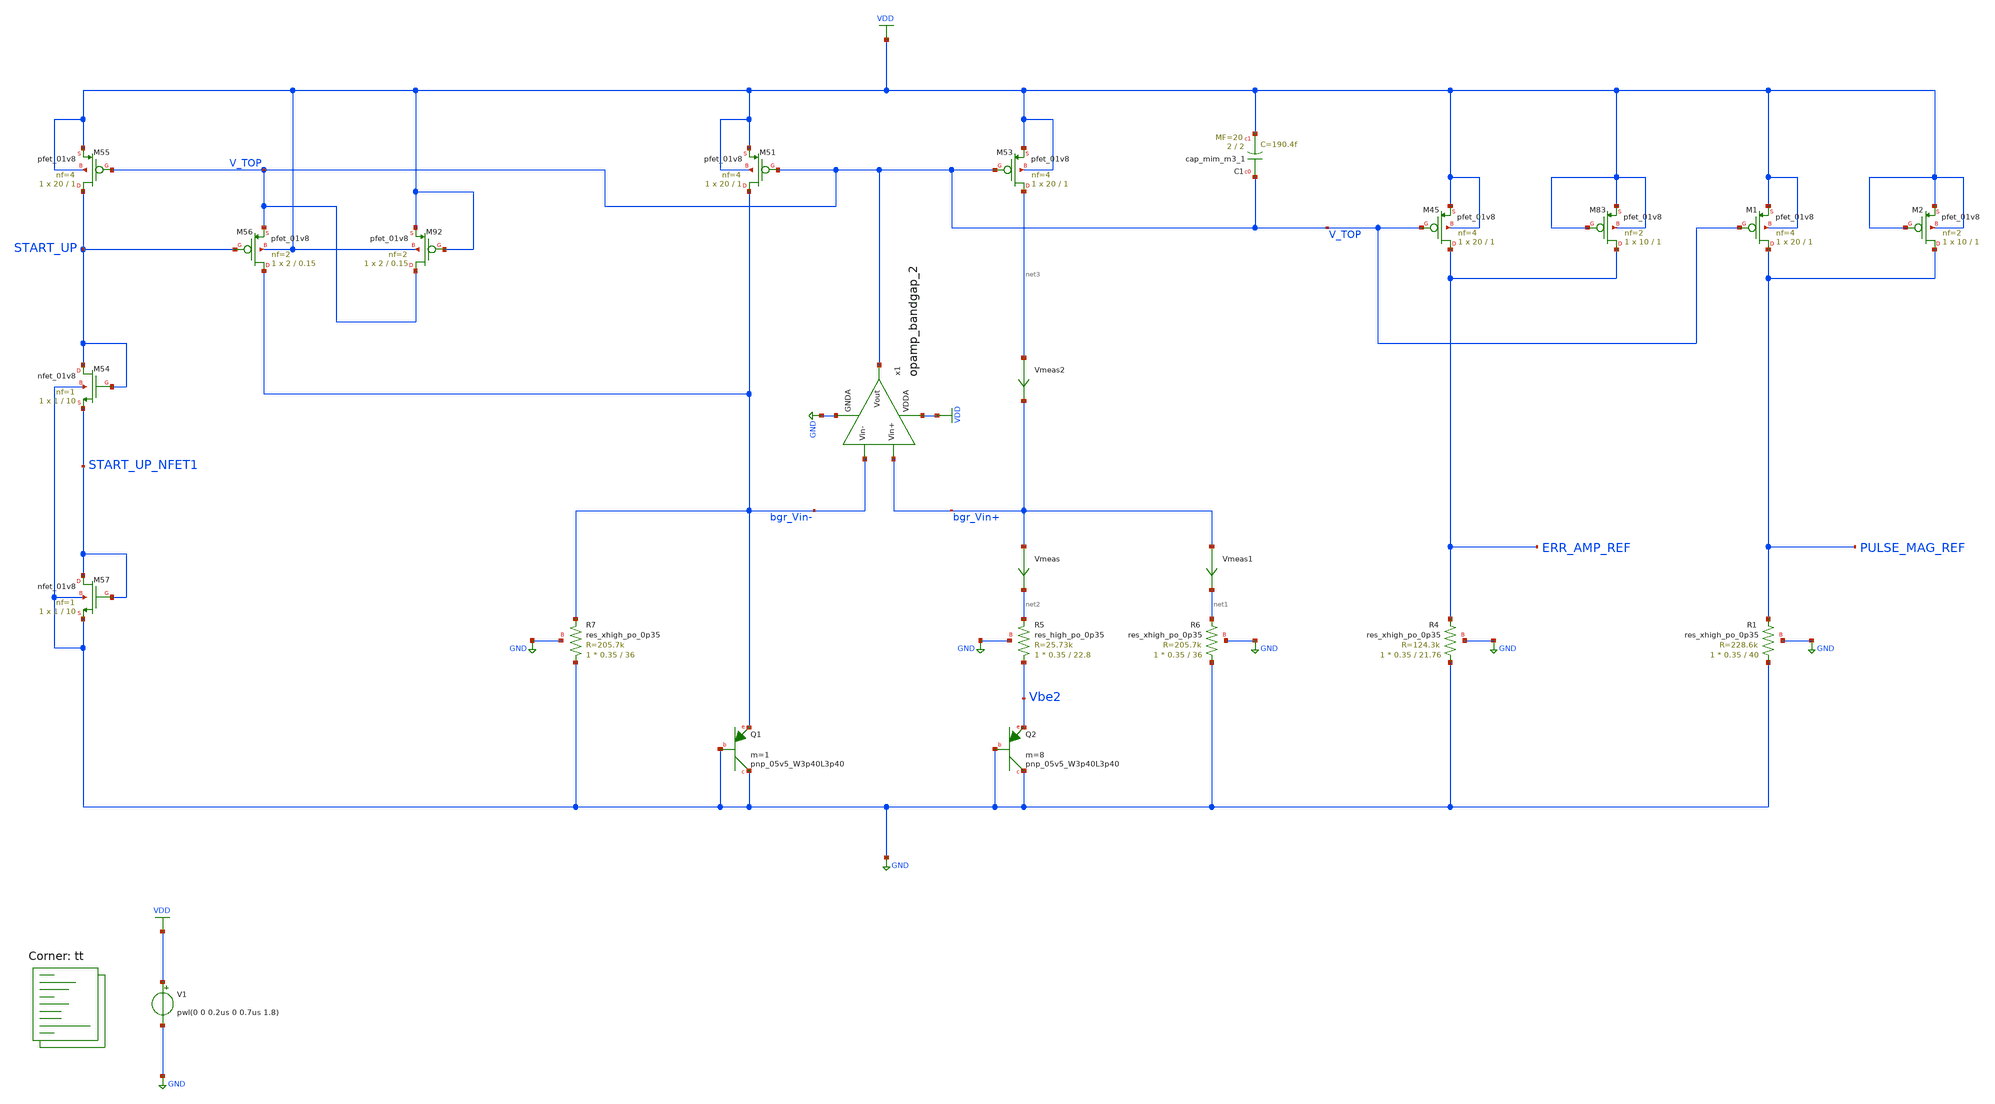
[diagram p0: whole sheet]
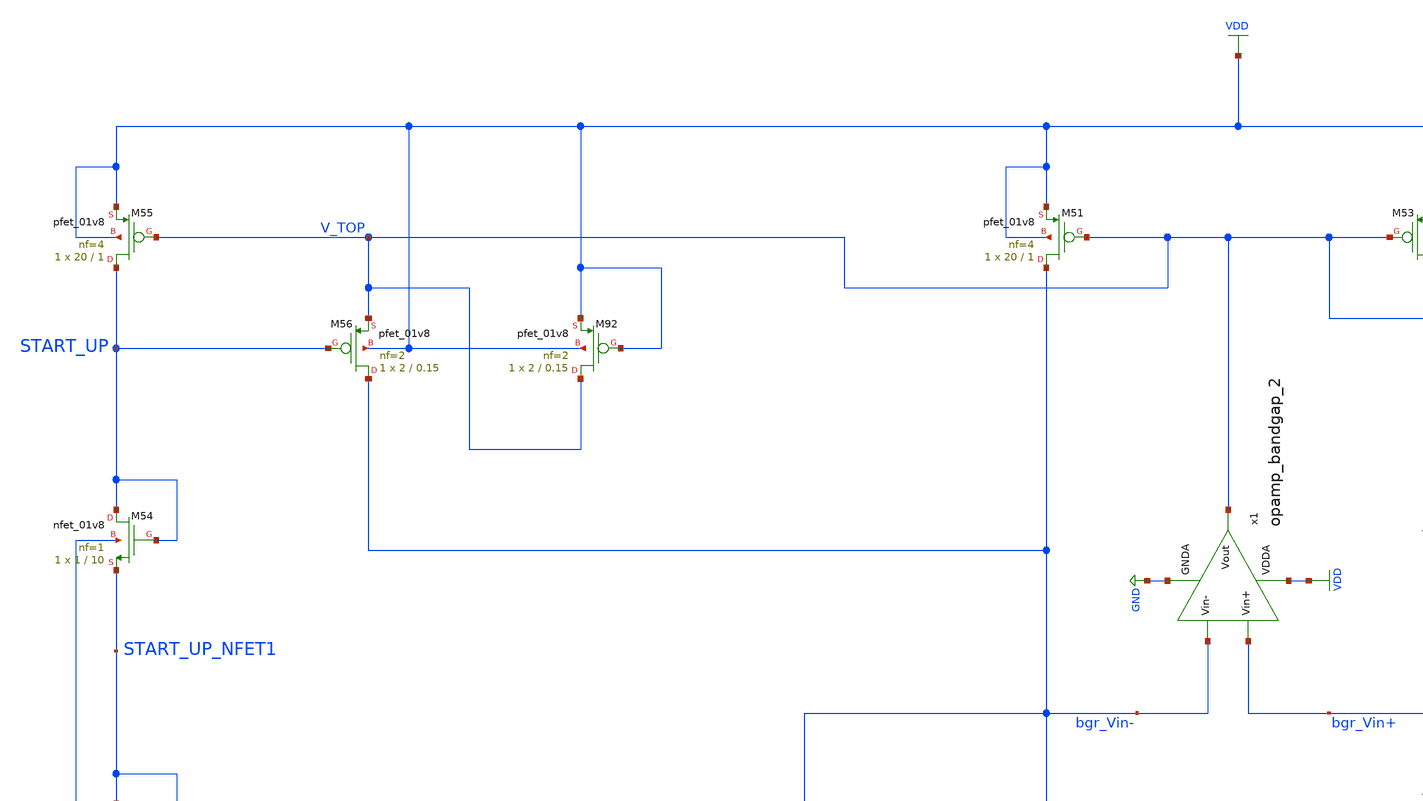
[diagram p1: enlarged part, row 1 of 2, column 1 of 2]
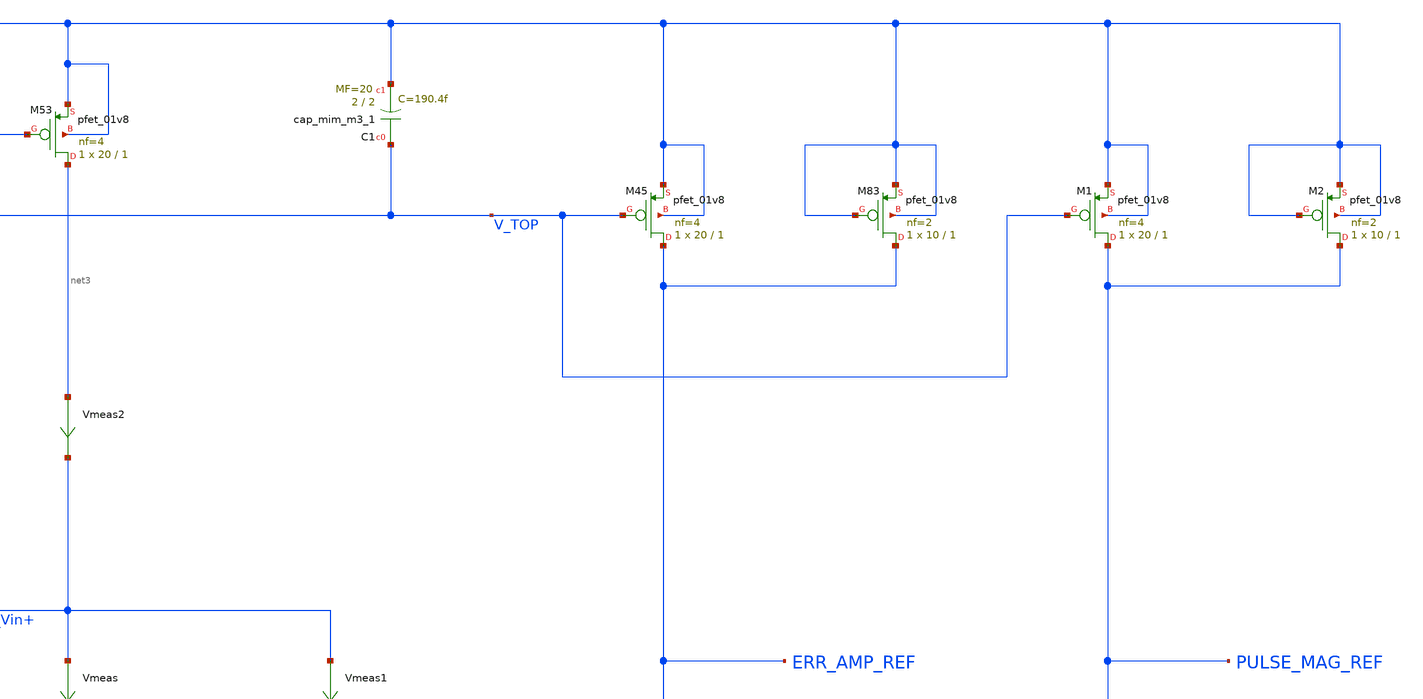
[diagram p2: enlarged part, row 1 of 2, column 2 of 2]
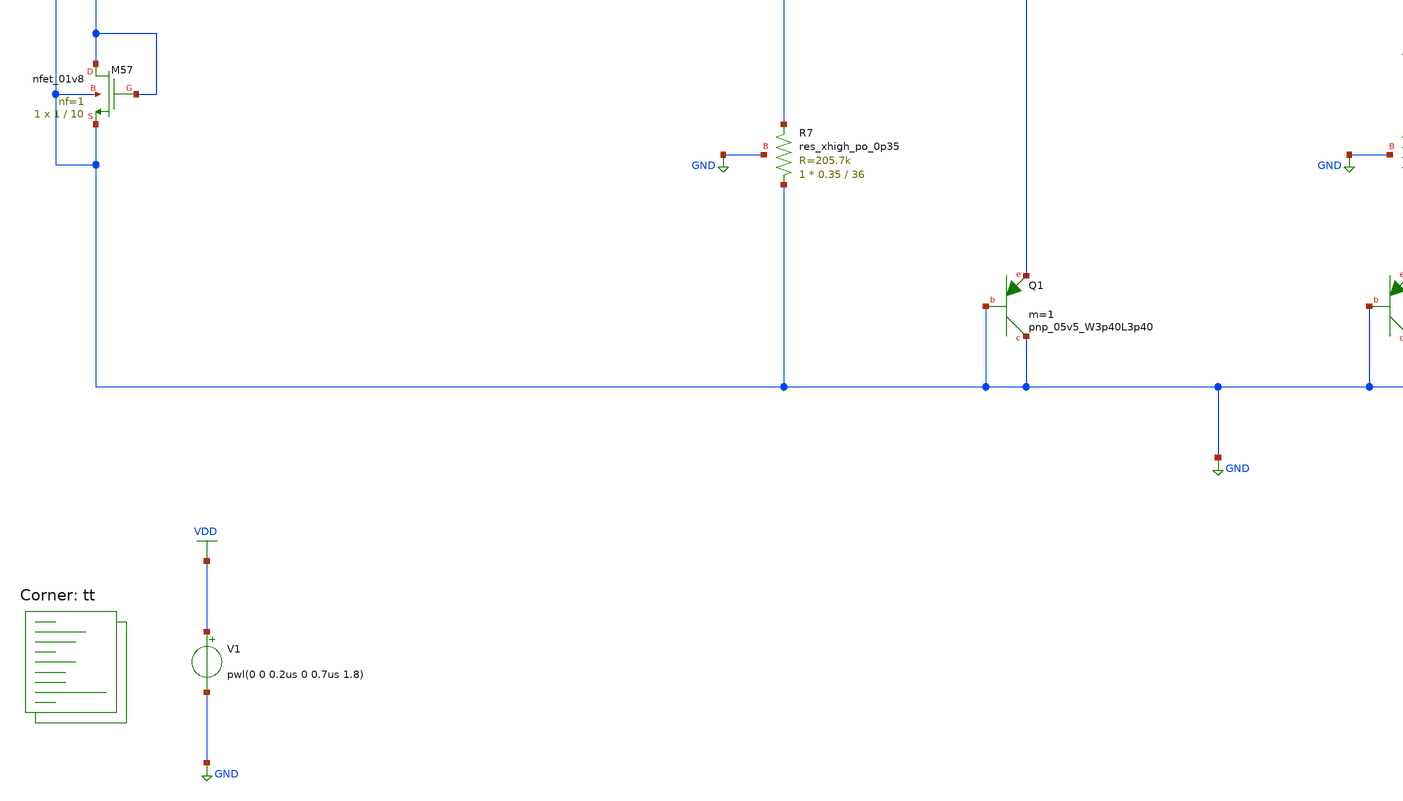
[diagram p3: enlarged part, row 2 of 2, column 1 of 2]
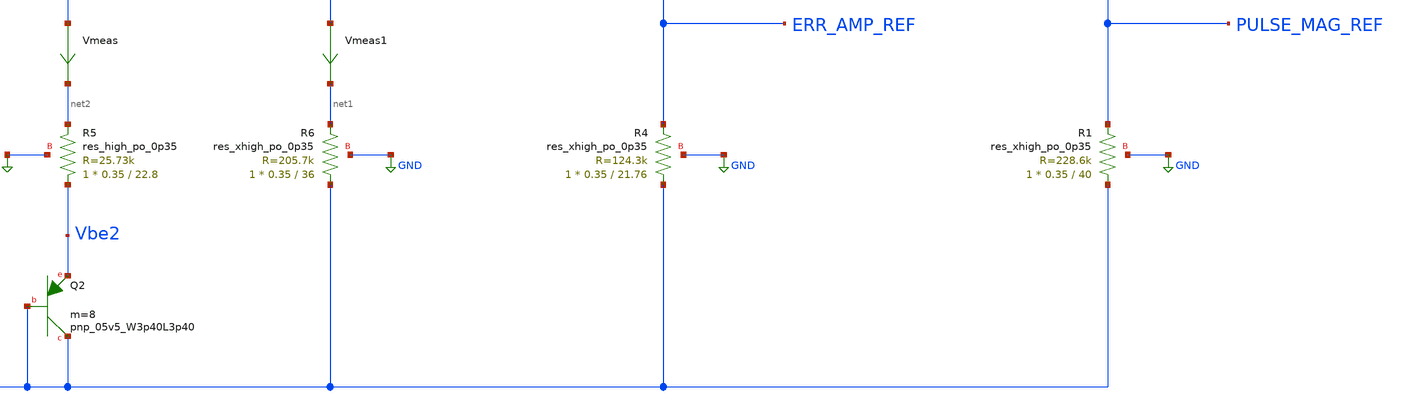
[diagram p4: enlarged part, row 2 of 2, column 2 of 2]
** sch_path: projects/ASU/EEE572/schematic/tb_ref_volt_cur_gen_dummy_2.sch
**.subckt tb_ref_volt_cur_gen_dummy_2
V1 VDD GND pwl(0 0 0.2us 0 0.7us 1.8)
XM45 ERR_AMP_REF V_TOP VDD VDD sky130_fd_pr__pfet_01v8 L=1 W=20 nf=4 ad='int((nf+1)/2) * W/nf * 0.29'
+ as='int((nf+2)/2) * W/nf * 0.29' pd='2*int((nf+1)/2) * (W/nf + 0.29)' ps='2*int((nf+2)/2) * (W/nf + 0.29)'
+ nrd='0.29 / W' nrs='0.29 / W' sa=0 sb=0 sd=0 mult=1 m=1
XR4 GND ERR_AMP_REF GND sky130_fd_pr__res_xhigh_po_0p35 L=21.76 mult=1 m=1
XC1 V_TOP VDD sky130_fd_pr__cap_mim_m3_1 W=2 L=2 MF=20 m=20
XQ1 GND GND bgr_Vin- sky130_fd_pr__pnp_05v5_W3p40L3p40 m=1
XQ2 GND GND Vbe2 sky130_fd_pr__pnp_05v5_W3p40L3p40 m=8
XM51 bgr_Vin- V_TOP VDD VDD sky130_fd_pr__pfet_01v8 L=1 W=20 nf=4 ad='int((nf+1)/2) * W/nf * 0.29' as='int((nf+2)/2) * W/nf * 0.29'
+ pd='2*int((nf+1)/2) * (W/nf + 0.29)' ps='2*int((nf+2)/2) * (W/nf + 0.29)' nrd='0.29 / W' nrs='0.29 / W'
+ sa=0 sb=0 sd=0 mult=1 m=1
XM53 net3 V_TOP VDD VDD sky130_fd_pr__pfet_01v8 L=1 W=20 nf=4 ad='int((nf+1)/2) * W/nf * 0.29' as='int((nf+2)/2) * W/nf * 0.29'
+ pd='2*int((nf+1)/2) * (W/nf + 0.29)' ps='2*int((nf+2)/2) * (W/nf + 0.29)' nrd='0.29 / W' nrs='0.29 / W'
+ sa=0 sb=0 sd=0 mult=1 m=1
XR6 GND net1 GND sky130_fd_pr__res_xhigh_po_0p35 L=36 mult=1 m=1
XR7 GND bgr_Vin- GND sky130_fd_pr__res_xhigh_po_0p35 L=36 mult=1 m=1
XM54 START_UP START_UP START_UP_NFET1 GND sky130_fd_pr__nfet_01v8 L=10 W=1 nf=1 ad='int((nf+1)/2) * W/nf * 0.29'
+ as='int((nf+2)/2) * W/nf * 0.29' pd='2*int((nf+1)/2) * (W/nf + 0.29)' ps='2*int((nf+2)/2) * (W/nf + 0.29)'
+ nrd='0.29 / W' nrs='0.29 / W' sa=0 sb=0 sd=0 mult=1 m=1
XM55 START_UP V_TOP VDD VDD sky130_fd_pr__pfet_01v8 L=1 W=20 nf=4 ad='int((nf+1)/2) * W/nf * 0.29' as='int((nf+2)/2) * W/nf * 0.29'
+ pd='2*int((nf+1)/2) * (W/nf + 0.29)' ps='2*int((nf+2)/2) * (W/nf + 0.29)' nrd='0.29 / W' nrs='0.29 / W'
+ sa=0 sb=0 sd=0 mult=1 m=1
XM56 bgr_Vin- START_UP V_TOP VDD sky130_fd_pr__pfet_01v8 L=0.15 W=2 nf=2 ad='int((nf+1)/2) * W/nf * 0.29'
+ as='int((nf+2)/2) * W/nf * 0.29' pd='2*int((nf+1)/2) * (W/nf + 0.29)' ps='2*int((nf+2)/2) * (W/nf + 0.29)'
+ nrd='0.29 / W' nrs='0.29 / W' sa=0 sb=0 sd=0 mult=1 m=1
XM57 START_UP_NFET1 START_UP_NFET1 GND GND sky130_fd_pr__nfet_01v8 L=10 W=1 nf=1 ad='int((nf+1)/2) * W/nf * 0.29'
+ as='int((nf+2)/2) * W/nf * 0.29' pd='2*int((nf+1)/2) * (W/nf + 0.29)' ps='2*int((nf+2)/2) * (W/nf + 0.29)'
+ nrd='0.29 / W' nrs='0.29 / W' sa=0 sb=0 sd=0 mult=1 m=1
x1 VDD V_TOP bgr_Vin- bgr_Vin+ GND opamp_bandgap_2
XM83 ERR_AMP_REF VDD VDD VDD sky130_fd_pr__pfet_01v8 L=1 W=10 nf=2 ad='int((nf+1)/2) * W/nf * 0.29' as='int((nf+2)/2) * W/nf * 0.29'
+ pd='2*int((nf+1)/2) * (W/nf + 0.29)' ps='2*int((nf+2)/2) * (W/nf + 0.29)' nrd='0.29 / W' nrs='0.29 / W'
+ sa=0 sb=0 sd=0 mult=1 m=1
XM92 V_TOP VDD VDD VDD sky130_fd_pr__pfet_01v8 L=0.15 W=2 nf=2 ad='int((nf+1)/2) * W/nf * 0.29' as='int((nf+2)/2) * W/nf * 0.29'
+ pd='2*int((nf+1)/2) * (W/nf + 0.29)' ps='2*int((nf+2)/2) * (W/nf + 0.29)' nrd='0.29 / W' nrs='0.29 / W'
+ sa=0 sb=0 sd=0 mult=1 m=1
XR5 Vbe2 net2 GND sky130_fd_pr__res_high_po_0p35 L=22.8 mult=1 m=1
XM1 PULSE_MAG_REF V_TOP VDD VDD sky130_fd_pr__pfet_01v8 L=1 W=20 nf=4 ad='int((nf+1)/2) * W/nf * 0.29'
+ as='int((nf+2)/2) * W/nf * 0.29' pd='2*int((nf+1)/2) * (W/nf + 0.29)' ps='2*int((nf+2)/2) * (W/nf + 0.29)'
+ nrd='0.29 / W' nrs='0.29 / W' sa=0 sb=0 sd=0 mult=1 m=1
XR1 GND PULSE_MAG_REF GND sky130_fd_pr__res_xhigh_po_0p35 L=40 mult=1 m=1
XM2 PULSE_MAG_REF VDD VDD VDD sky130_fd_pr__pfet_01v8 L=1 W=10 nf=2 ad='int((nf+1)/2) * W/nf * 0.29'
+ as='int((nf+2)/2) * W/nf * 0.29' pd='2*int((nf+1)/2) * (W/nf + 0.29)' ps='2*int((nf+2)/2) * (W/nf + 0.29)'
+ nrd='0.29 / W' nrs='0.29 / W' sa=0 sb=0 sd=0 mult=1 m=1
Vmeas bgr_Vin+ net2 0
.save i(vmeas)
Vmeas1 bgr_Vin+ net1 0
.save i(vmeas1)
Vmeas2 net3 bgr_Vin+ 0
.save i(vmeas2)
**** begin user architecture code
.lib $::SKYWATER_MODELS/sky130.lib.spice tt



* ngspice commands


.option method=gear
.option wnflag=1
.option savecurrents
* .temp =140

.save @m.xm1.msky130_fd_pr__pfet_01v8[gm] @m.xm1.msky130_fd_pr__pfet_01v8[vth] @m.xm1.msky130_fd_pr__pfet_01v8[vgs] @m.xm1.msky130_fd_pr__pfet_01v8[vds] @m.xm2.msky130_fd_pr__pfet_01v8[gm] @m.xm2.msky130_fd_pr__pfet_01v8[vth] @m.xm2.msky130_fd_pr__pfet_01v8[vgs] @m.xm2.msky130_fd_pr__pfet_01v8[vds] @m.xm3.msky130_fd_pr__pfet_01v8[gm] @m.xm4.msky130_fd_pr__pfet_01v8[gm] @m.xm4.msky130_fd_pr__pfet_01v8[vth] @m.xm5.msky130_fd_pr__nfet_01v8[gm] @m.xm5.msky130_fd_pr__nfet_01v8[vth] @m.xm6.msky130_fd_pr__pfet_01v8[gm] @m.xm6.msky130_fd_pr__pfet_01v8[vth] @m.xm7.msky130_fd_pr__nfet_01v8[gm] @m.xm7.msky130_fd_pr__nfet_01v8[vth] @m.xm8.msky130_fd_pr__nfet_01v8[gm] @m.xm8.msky130_fd_pr__nfet_01v8[vth] @m.xm9.msky130_fd_pr__nfet_01v8[gm] @m.xm9.msky130_fd_pr__nfet_01v8[vth] @m.x1.xm1.msky130_fd_pr__nfet_01v8[gm] @m.x1.xm2.msky130_fd_pr__nfet_01v8[gm] @m.x1.xm3.msky130_fd_pr__nfet_01v8[gm] @m.x1.xm4.msky130_fd_pr__nfet_01v8[gm] @m.x1.xm5.msky130_fd_pr__pfet_01v8[gm] @m.x1.xm6.msky130_fd_pr__nfet_01v8[gm] @m.x1.xm7.msky130_fd_pr__pfet_01v8[gm]

* .ic v(vin-) = 0.8
* .ic v(vin+) = 0.8
* .ic v(v_top) = 1.8

.control

    save all
    * dc temp -40 120 5 V1 1.6 2.0 0.05
    * dc V1 1.7 1.9 0.001 temp -40 120 40
    * dc V1 0.0 2.0 0.02 temp -40 120 20
    * dc V1 0 2.0 0.02
    tran 20ps 1us
    * tran 10ns 10us
    remzerovec
    write tb_ref_volt_cur_gen_dummy_2.raw
.endc




**** end user architecture code
**.ends

* expanding   symbol:
*+  /foss/designs/my_design/projects/bandgapref/xschem_ngspice/new_files/opamp_bandgap_2.sym # of pins=5
** sym_path: projects/bandgapref/xschem_ngspice/new_files/opamp_bandgap_2.sym
** sch_path: projects/bandgapref/xschem_ngspice/new_files/opamp_bandgap_2.sch
.subckt opamp_bandgap_2 VDDA Vout Vin- Vin+ GNDA
*.ipin Vin+
*.opin Vout
*.ipin Vin-
*.ipin GNDA
*.ipin VDDA
XM1 V_p VDDA GNDA GNDA sky130_fd_pr__nfet_01v8 L=10 W=5 nf=1 ad='int((nf+1)/2) * W/nf * 0.29' as='int((nf+2)/2) * W/nf * 0.29'
+ pd='2*int((nf+1)/2) * (W/nf + 0.29)' ps='2*int((nf+2)/2) * (W/nf + 0.29)' nrd='0.29 / W' nrs='0.29 / W'
+ sa=0 sb=0 sd=0 mult=1 m=1
XM2 V_mirror Vin- V_p GNDA sky130_fd_pr__nfet_01v8 L=0.2 W=5 nf=1 ad='int((nf+1)/2) * W/nf * 0.29' as='int((nf+2)/2) * W/nf * 0.29'
+ pd='2*int((nf+1)/2) * (W/nf + 0.29)' ps='2*int((nf+2)/2) * (W/nf + 0.29)' nrd='0.29 / W' nrs='0.29 / W'
+ sa=0 sb=0 sd=0 mult=1 m=1
XM3 1st_Vout Vin+ V_p GNDA sky130_fd_pr__nfet_01v8 L=0.2 W=5 nf=1 ad='int((nf+1)/2) * W/nf * 0.29' as='int((nf+2)/2) * W/nf * 0.29'
+ pd='2*int((nf+1)/2) * (W/nf + 0.29)' ps='2*int((nf+2)/2) * (W/nf + 0.29)' nrd='0.29 / W' nrs='0.29 / W'
+ sa=0 sb=0 sd=0 mult=1 m=1
XM5 V_mirror V_mirror VDDA VDDA sky130_fd_pr__pfet_01v8 L=0.2 W=10 nf=2 ad='int((nf+1)/2) * W/nf * 0.29'
+ as='int((nf+2)/2) * W/nf * 0.29' pd='2*int((nf+1)/2) * (W/nf + 0.29)' ps='2*int((nf+2)/2) * (W/nf + 0.29)'
+ nrd='0.29 / W' nrs='0.29 / W' sa=0 sb=0 sd=0 mult=1 m=1
XM6 1st_Vout V_mirror VDDA VDDA sky130_fd_pr__pfet_01v8 L=0.2 W=10 nf=2 ad='int((nf+1)/2) * W/nf * 0.29'
+ as='int((nf+2)/2) * W/nf * 0.29' pd='2*int((nf+1)/2) * (W/nf + 0.29)' ps='2*int((nf+2)/2) * (W/nf + 0.29)'
+ nrd='0.29 / W' nrs='0.29 / W' sa=0 sb=0 sd=0 mult=1 m=1
XM4 Vout VDDA GNDA GNDA sky130_fd_pr__nfet_01v8 L=10 W=5 nf=1 ad='int((nf+1)/2) * W/nf * 0.29' as='int((nf+2)/2) * W/nf * 0.29'
+ pd='2*int((nf+1)/2) * (W/nf + 0.29)' ps='2*int((nf+2)/2) * (W/nf + 0.29)' nrd='0.29 / W' nrs='0.29 / W'
+ sa=0 sb=0 sd=0 mult=1 m=1
XM7 Vout 1st_Vout VDDA VDDA sky130_fd_pr__pfet_01v8 L=0.2 W=10 nf=2 ad='int((nf+1)/2) * W/nf * 0.29'
+ as='int((nf+2)/2) * W/nf * 0.29' pd='2*int((nf+1)/2) * (W/nf + 0.29)' ps='2*int((nf+2)/2) * (W/nf + 0.29)'
+ nrd='0.29 / W' nrs='0.29 / W' sa=0 sb=0 sd=0 mult=1 m=1
.ends

.GLOBAL GND
.GLOBAL VDD
.end
